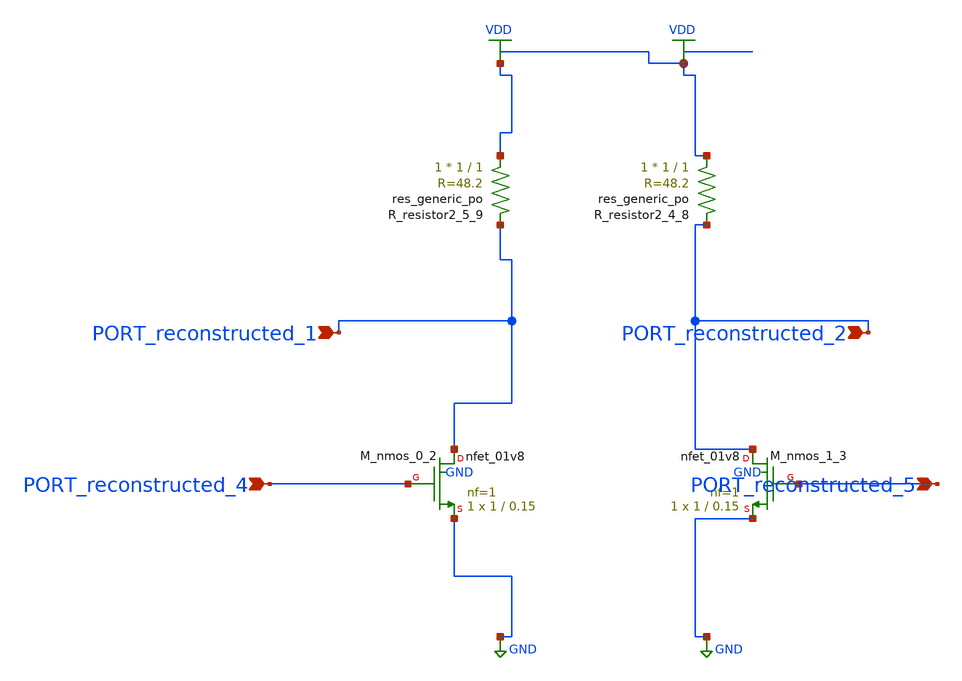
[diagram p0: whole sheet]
** sch_path: schematics/AMSNet/188.sch
**.subckt 188 PORT_reconstructed_5 PORT_reconstructed_4 PORT_reconstructed_1 PORT_reconstructed_2
*.ipin PORT_reconstructed_5
*.ipin PORT_reconstructed_4
*.ipin PORT_reconstructed_1
*.ipin PORT_reconstructed_2
XM_nmos_0_2 PORT_reconstructed_1 PORT_reconstructed_4 GND GND sky130_fd_pr__nfet_01v8 L=0.15 W=1 nf=1
+ ad='int((1 + 1)/2) * 1 / 1 * 0.29' as='int((1 + 2)/2) * 1 / 1 * 0.29' pd='2*int((1 + 1)/2) * (1 / 1 + 0.29)'
+ ps='2*int((1 + 2)/2) * (1 / 1 + 0.29)' nrd='0.29 / 1 ' nrs='0.29 / 1 ' sa=0 sb=0 sd=0 mult=1 m=1
XM_nmos_1_3 PORT_reconstructed_2 PORT_reconstructed_5 GND GND sky130_fd_pr__nfet_01v8 L=0.15 W=1 nf=1
+ ad='int((1 + 1)/2) * 1 / 1 * 0.29' as='int((1 + 2)/2) * 1 / 1 * 0.29' pd='2*int((1 + 1)/2) * (1 / 1 + 0.29)'
+ ps='2*int((1 + 2)/2) * (1 / 1 + 0.29)' nrd='0.29 / 1 ' nrs='0.29 / 1 ' sa=0 sb=0 sd=0 mult=1 m=1
XR_resistor2_4_8 VDD PORT_reconstructed_2 sky130_fd_pr__res_generic_po W=1 L=1 m=1
XR_resistor2_5_9 VDD PORT_reconstructed_1 sky130_fd_pr__res_generic_po W=1 L=1 m=1
**.ends
.GLOBAL GND
.GLOBAL VDD
.end
